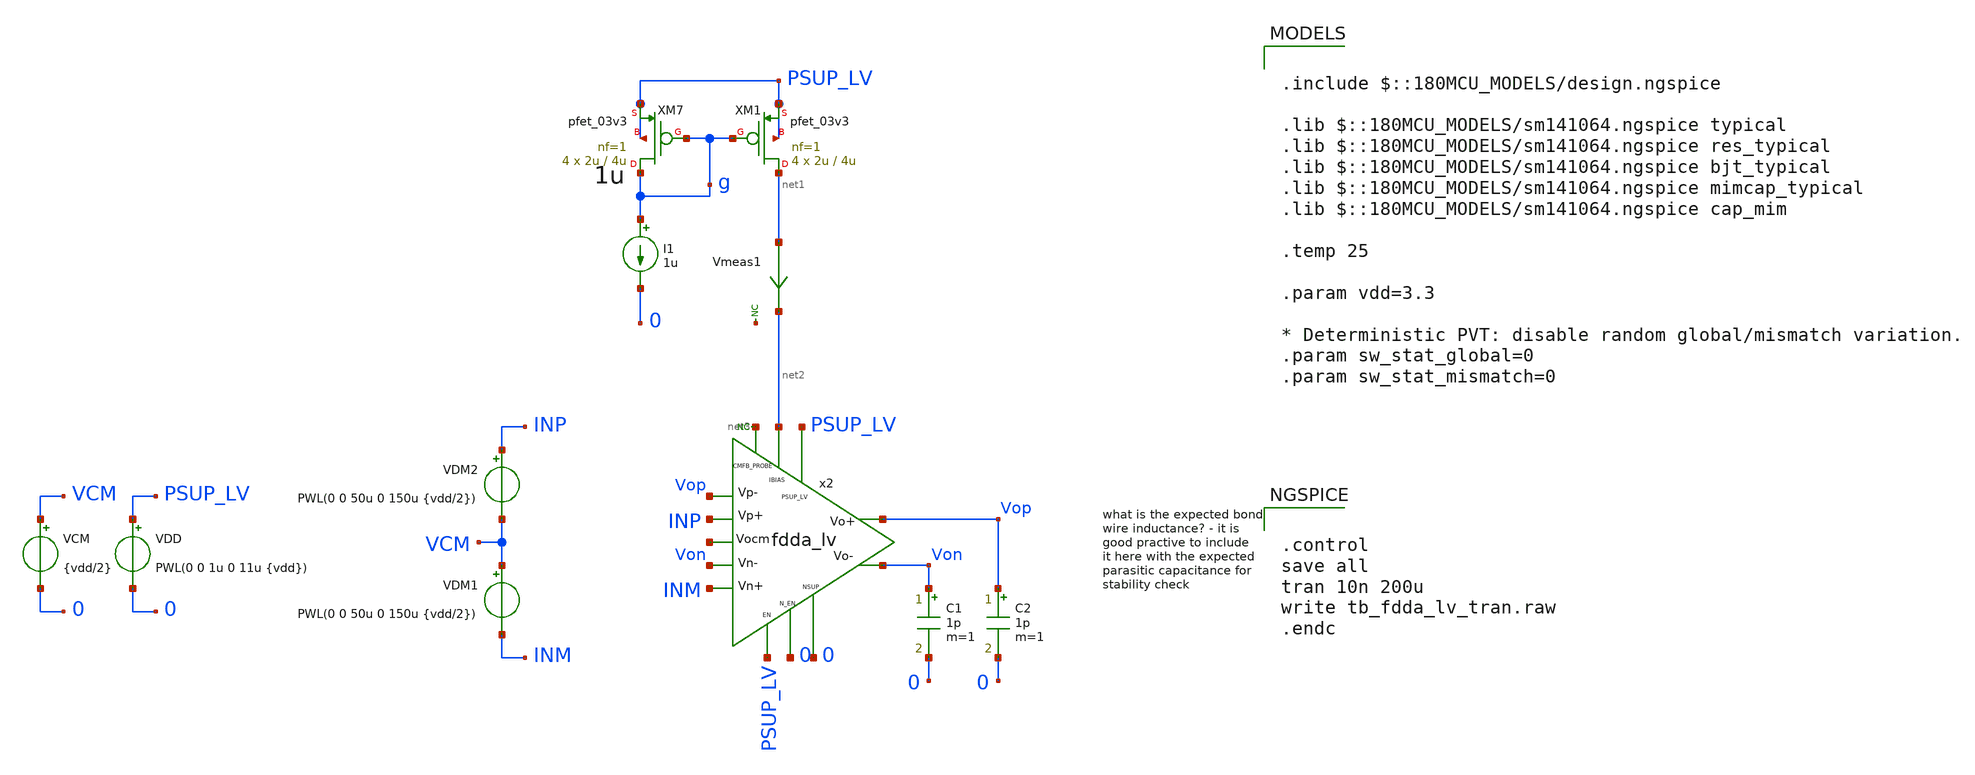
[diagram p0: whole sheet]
** sch_path: xschem/blocks/fdda_lv/tb_fdda_lv_tran.sch
**.subckt tb_fdda_lv_tran
C1 Von 0 1p m=1
x2 PSUP_LV Vop Von INM INP Vop Von net2 0 PSUP_LV 0 net3 net4 fdda_lv
VDD PSUP_LV 0 PWL(0 0 1u 0 11u {vdd})
C2 Vop 0 1p m=1
VCM VCM 0 {vdd/2}
VDM2 INP VCM PWL(0 0 50u 0 150u {vdd/2})
VDM1 VCM INM PWL(0 0 50u 0 150u {vdd/2})
* noconn #net3
* noconn #net5
XM7 g g PSUP_LV PSUP_LV pfet_03v3 L=4u W=2u nf=1 ad='int((nf+1)/2) * W/nf * 0.18u' as='int((nf+2)/2) * W/nf * 0.18u'
+ pd='2*int((nf+1)/2) * (W/nf + 0.18u)' ps='2*int((nf+2)/2) * (W/nf + 0.18u)' nrd='0.18u / W' nrs='0.18u / W'
+ sa=0 sb=0 sd=0 m=4
XM1 net1 g PSUP_LV PSUP_LV pfet_03v3 L=4u W=2u nf=1 ad='int((nf+1)/2) * W/nf * 0.18u' as='int((nf+2)/2) * W/nf * 0.18u'
+ pd='2*int((nf+1)/2) * (W/nf + 0.18u)' ps='2*int((nf+2)/2) * (W/nf + 0.18u)' nrd='0.18u / W' nrs='0.18u / W'
+ sa=0 sb=0 sd=0 m=4
I1 g 0 1u
Vmeas1 net1 net2 0
.save i(vmeas1)
**** begin user architecture code

.include $::180MCU_MODELS/design.ngspice

.lib $::180MCU_MODELS/sm141064.ngspice typical
.lib $::180MCU_MODELS/sm141064.ngspice res_typical
.lib $::180MCU_MODELS/sm141064.ngspice bjt_typical
.lib $::180MCU_MODELS/sm141064.ngspice mimcap_typical
.lib $::180MCU_MODELS/sm141064.ngspice cap_mim

.temp 25

.param vdd=3.3

* Deterministic PVT: disable random global/mismatch variation.
.param sw_stat_global=0
.param sw_stat_mismatch=0



.control
save all
tran 10n 200u
write tb_fdda_lv_tran.raw
.endc


**** end user architecture code
**.ends
.end
